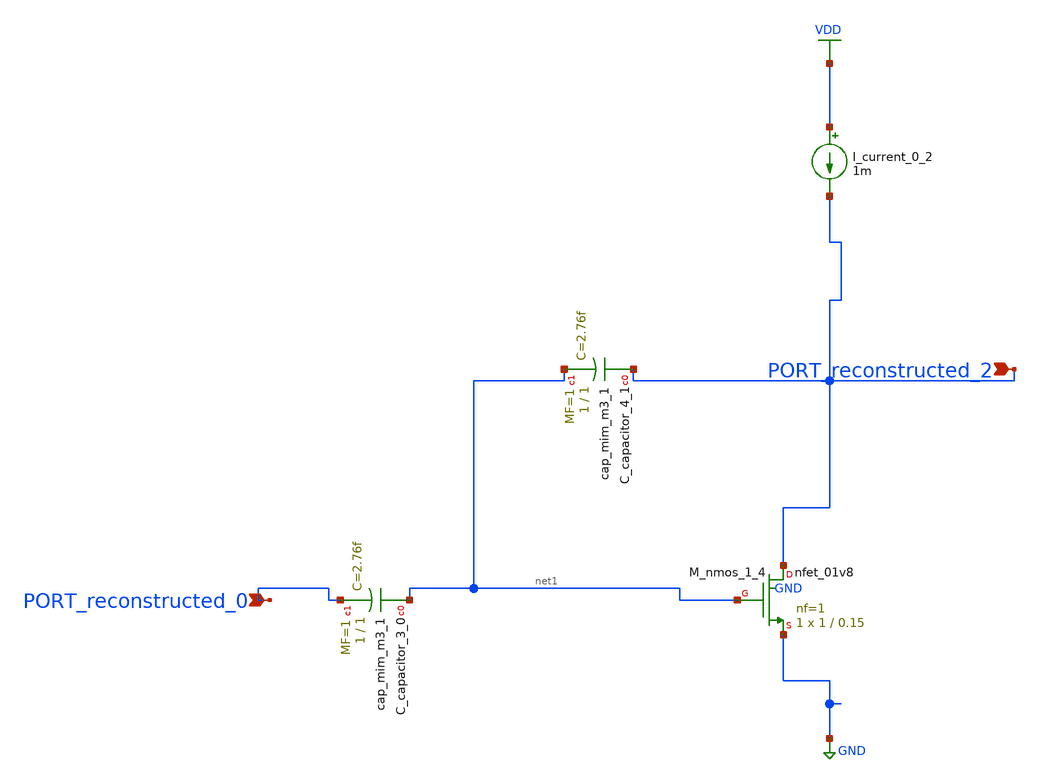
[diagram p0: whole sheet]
** sch_path: schematics/AMSNet/536.sch
**.subckt 536 PORT_reconstructed_2 PORT_reconstructed_0
*.ipin PORT_reconstructed_2
*.ipin PORT_reconstructed_0
XC_capacitor_3_0 net1 PORT_reconstructed_0 sky130_fd_pr__cap_mim_m3_1 W=1 L=1 MF=1 m=1
XC_capacitor_4_1 PORT_reconstructed_2 net1 sky130_fd_pr__cap_mim_m3_1 W=1 L=1 MF=1 m=1
I_current_0_2 VDD PORT_reconstructed_2 1m
XM_nmos_1_4 PORT_reconstructed_2 net1 GND GND sky130_fd_pr__nfet_01v8 L=0.15 W=1 nf=1 ad='int((1 + 1)/2) * 1 / 1 * 0.29'
+ as='int((1 + 2)/2) * 1 / 1 * 0.29' pd='2*int((1 + 1)/2) * (1 / 1 + 0.29)' ps='2*int((1 + 2)/2) * (1 / 1 + 0.29)'
+ nrd='0.29 / 1 ' nrs='0.29 / 1 ' sa=0 sb=0 sd=0 mult=1 m=1
**.ends
.GLOBAL GND
.GLOBAL VDD
.end
